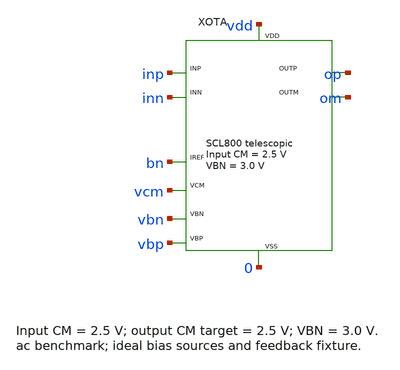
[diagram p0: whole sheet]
** sch_path: OTA/final_design/designs/ota_cm2p5_ac_tb.sch
**.subckt ota_cm2p5_ac_tb
XOTA inp inn op om vdd 0 bn vcm vbn vbp ota_telescopic_cm2p5
**** begin user architecture code

.include ../models/scl08_models.inc
.include ../models/ota_cm2p5_C.spice
.temp 27
.options reltol=1e-5 vntol=1e-8 abstol=1e-12
VDD vdd 0 5
IREF vdd bn 3.5u
VCM vcm 0 2.5
VBN vbn 0 3
VBP vbp vdd -2.2
CLP op 0 5p
CLM om 0 5p
VCMD cmd 0 dc 0 ac 1
VICM icm 0 2.5
EIP inp icm cmd fb 0.5
EIM inn icm fb cmd 0.5
EOD od 0 op om 1
LDC od fb 1e12
CAC fb 0 1e12
.control
set wr_singlescale
set wr_vecnames
op
print v(op) v(om) i(vdd)
ac dec 80 0.01 1G
let gr=real(v(od))
let gi=imag(v(od))
wrdata ac.dat gr gi
write ota_cm2p5_ac.raw
quit
.endc

**** end user architecture code
**.ends
.end
